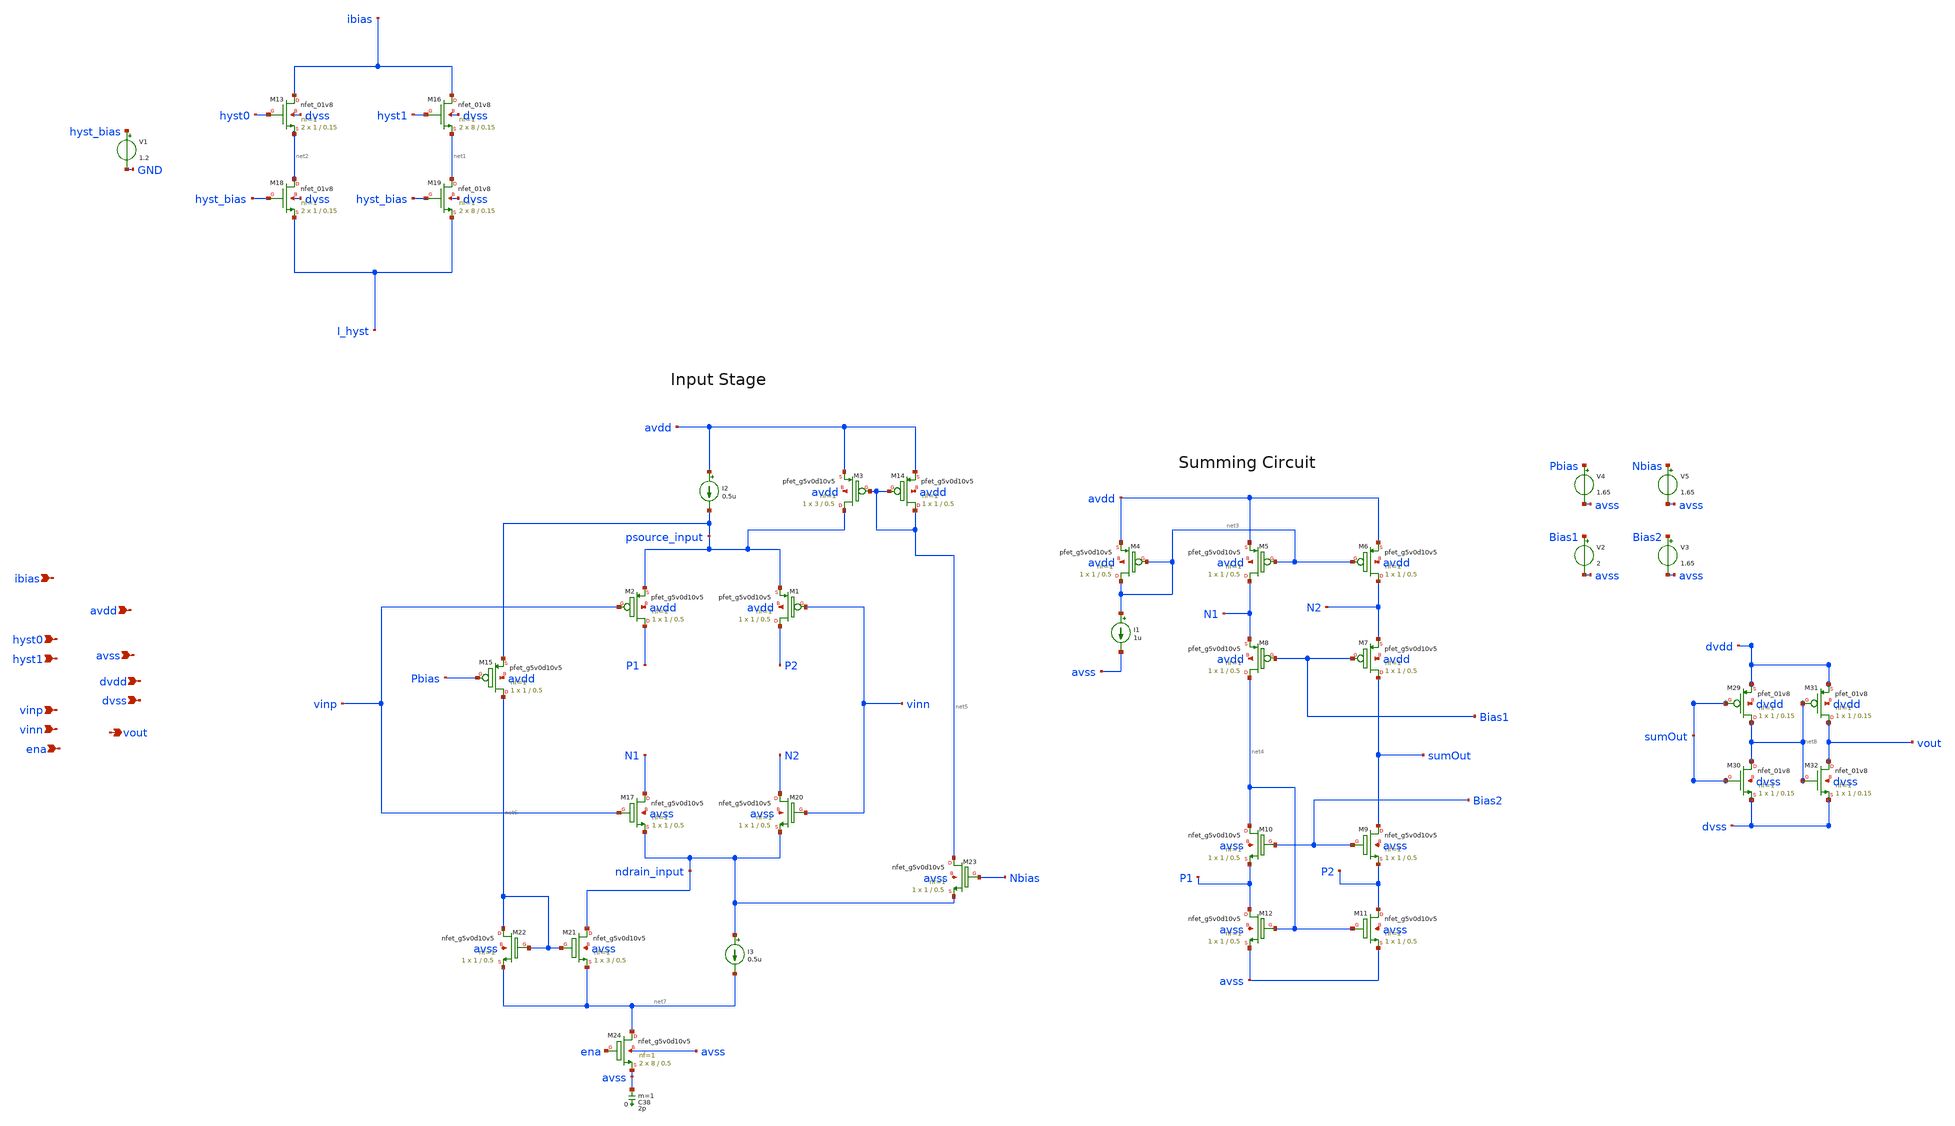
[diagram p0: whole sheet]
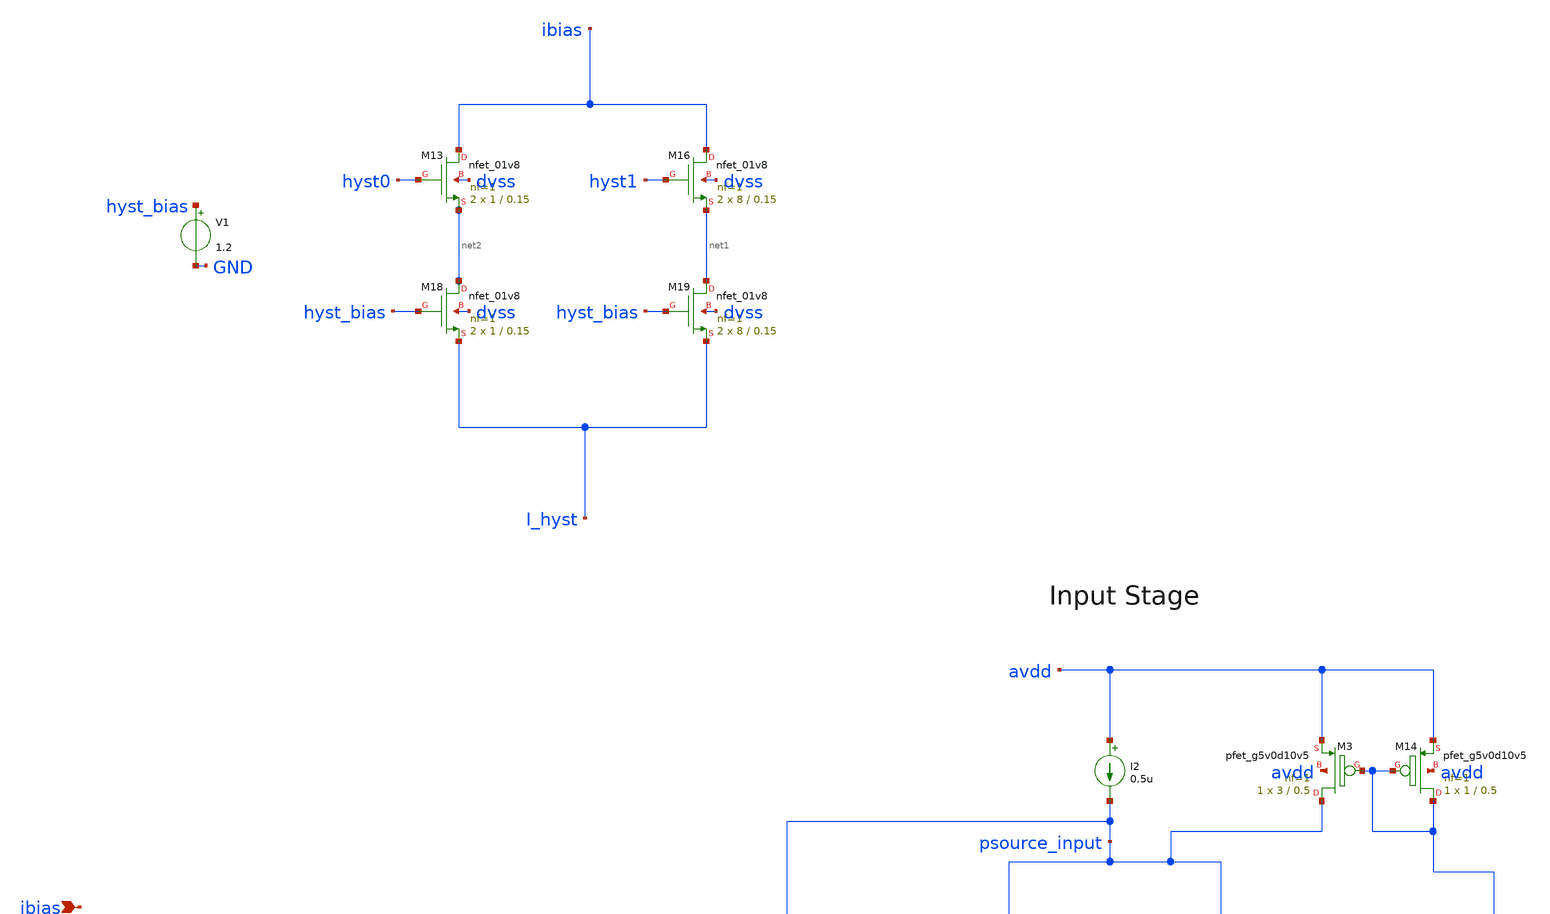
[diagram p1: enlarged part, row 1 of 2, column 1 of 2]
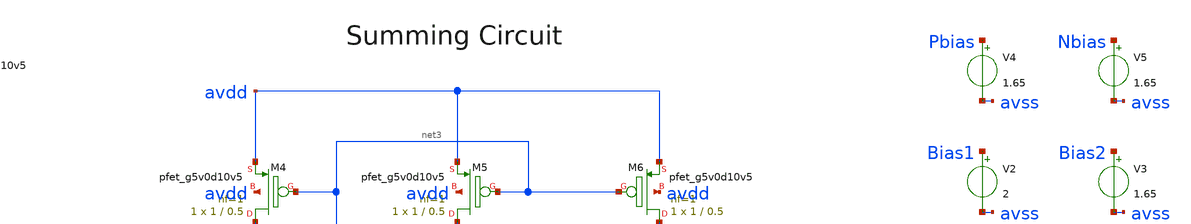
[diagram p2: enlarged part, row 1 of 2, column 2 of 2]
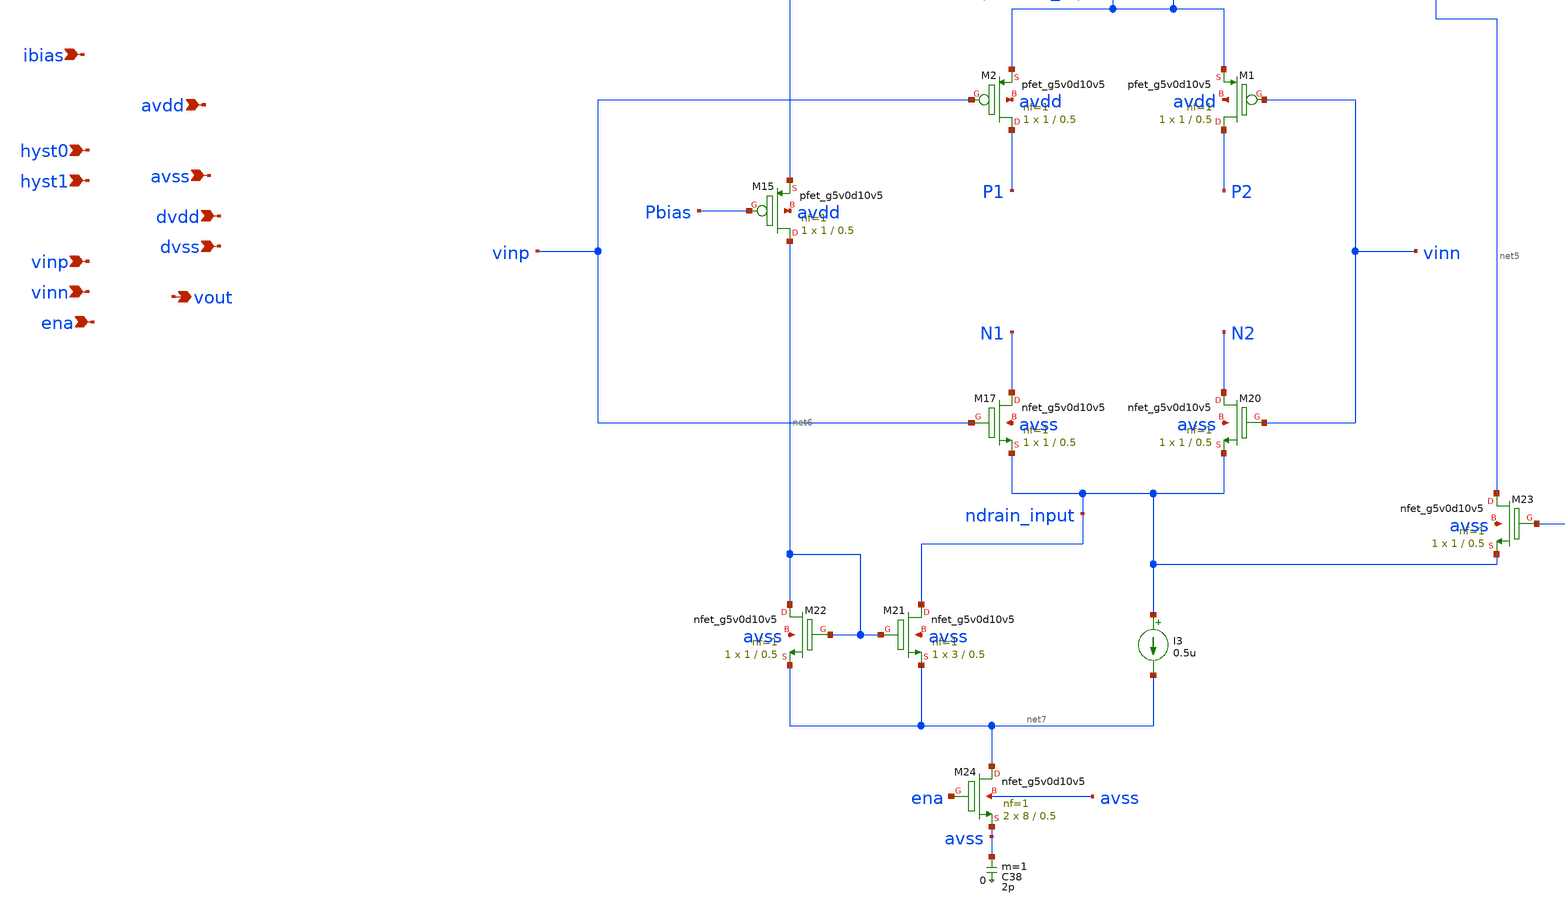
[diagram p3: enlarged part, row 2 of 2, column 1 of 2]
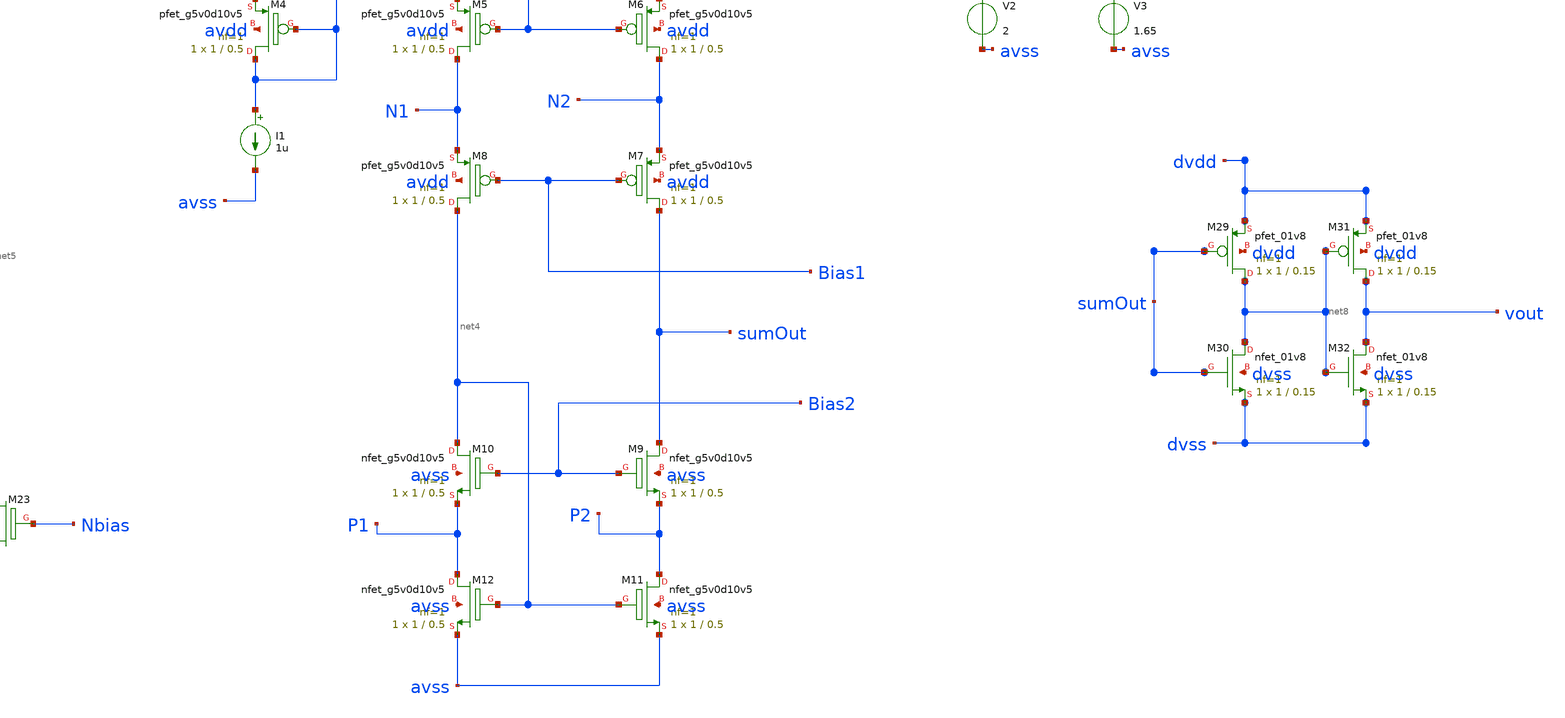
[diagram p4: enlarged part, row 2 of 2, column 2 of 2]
** sch_path: Chipalooza_April2024_Comparator/xschem/Chipalooza_April2024_Comparator(copy2).sch
**.subckt Chipalooza_April2024_Comparator(copy2) vinp vinn hyst0 hyst1 avdd avss dvdd dvss vout ena
*+ ibias
*.ipin vinp
*.ipin vinn
*.ipin hyst0
*.ipin hyst1
*.ipin avdd
*.ipin avss
*.ipin dvdd
*.ipin dvss
*.opin vout
*.ipin ena
*.ipin ibias
XM13 ibias hyst0 net2 dvss sky130_fd_pr__nfet_01v8 L=0.15 W=1 nf=1 ad='int((1 + 1)/2) * 1 / 1 * 0.29'
+ as='int((1 + 2)/2) * 1 / 1 * 0.29' pd='2*int((1 + 1)/2) * (1 / 1 + 0.29)' ps='2*int((1 + 2)/2) * (1 / 1 + 0.29)'
+ nrd='0.29 / 1 ' nrs='0.29 / 1 ' sa=0 sb=0 sd=0 mult=2 m=2
C38 avss 0 2p m=1
XM24 net7 ena avss avss sky130_fd_pr__nfet_g5v0d10v5 L=0.5 W=8 nf=1 ad='int((nf+1)/2) * W/nf * 0.29'
+ as='int((nf+2)/2) * W/nf * 0.29' pd='2*int((nf+1)/2) * (W/nf + 0.29)' ps='2*int((nf+2)/2) * (W/nf + 0.29)'
+ nrd='0.29 / W' nrs='0.29 / W' sa=0 sb=0 sd=0 mult=2 m=2
XM16 ibias hyst1 net1 dvss sky130_fd_pr__nfet_01v8 L=0.15 W=8 nf=1 ad='int((1 + 1)/2) * 8 / 1 * 0.29'
+ as='int((1 + 2)/2) * 8 / 1 * 0.29' pd='2*int((1 + 1)/2) * (8 / 1 + 0.29)' ps='2*int((1 + 2)/2) * (8 / 1 + 0.29)'
+ nrd='0.29 / 8 ' nrs='0.29 / 8 ' sa=0 sb=0 sd=0 mult=2 m=2
XM19 net1 hyst_bias I_hyst dvss sky130_fd_pr__nfet_01v8 L=0.15 W=8 nf=1 ad='int((1 + 1)/2) * 8 / 1 * 0.29'
+ as='int((1 + 2)/2) * 8 / 1 * 0.29' pd='2*int((1 + 1)/2) * (8 / 1 + 0.29)' ps='2*int((1 + 2)/2) * (8 / 1 + 0.29)'
+ nrd='0.29 / 8 ' nrs='0.29 / 8 ' sa=0 sb=0 sd=0 mult=2 m=2
XM18 net2 hyst_bias I_hyst dvss sky130_fd_pr__nfet_01v8 L=0.15 W=1 nf=1 ad='int((1 + 1)/2) * 1 / 1 * 0.29'
+ as='int((1 + 2)/2) * 1 / 1 * 0.29' pd='2*int((1 + 1)/2) * (1 / 1 + 0.29)' ps='2*int((1 + 2)/2) * (1 / 1 + 0.29)'
+ nrd='0.29 / 1 ' nrs='0.29 / 1 ' sa=0 sb=0 sd=0 mult=2 m=2
V1 hyst_bias GND 1.2
XM4 net3 net3 avdd avdd sky130_fd_pr__pfet_g5v0d10v5 L=0.5 W=1 nf=1 ad='int((nf+1)/2) * W/nf * 0.29'
+ as='int((nf+2)/2) * W/nf * 0.29' pd='2*int((nf+1)/2) * (W/nf + 0.29)' ps='2*int((nf+2)/2) * (W/nf + 0.29)'
+ nrd='0.29 / W' nrs='0.29 / W' sa=0 sb=0 sd=0 mult=1 m=1
XM5 N1 net3 avdd avdd sky130_fd_pr__pfet_g5v0d10v5 L=0.5 W=1 nf=1 ad='int((nf+1)/2) * W/nf * 0.29' as='int((nf+2)/2) * W/nf * 0.29'
+ pd='2*int((nf+1)/2) * (W/nf + 0.29)' ps='2*int((nf+2)/2) * (W/nf + 0.29)' nrd='0.29 / W' nrs='0.29 / W'
+ sa=0 sb=0 sd=0 mult=1 m=1
XM6 N2 net3 avdd avdd sky130_fd_pr__pfet_g5v0d10v5 L=0.5 W=1 nf=1 ad='int((nf+1)/2) * W/nf * 0.29' as='int((nf+2)/2) * W/nf * 0.29'
+ pd='2*int((nf+1)/2) * (W/nf + 0.29)' ps='2*int((nf+2)/2) * (W/nf + 0.29)' nrd='0.29 / W' nrs='0.29 / W'
+ sa=0 sb=0 sd=0 mult=1 m=1
XM7 sumOut Bias1 N2 avdd sky130_fd_pr__pfet_g5v0d10v5 L=0.5 W=1 nf=1 ad='int((nf+1)/2) * W/nf * 0.29'
+ as='int((nf+2)/2) * W/nf * 0.29' pd='2*int((nf+1)/2) * (W/nf + 0.29)' ps='2*int((nf+2)/2) * (W/nf + 0.29)'
+ nrd='0.29 / W' nrs='0.29 / W' sa=0 sb=0 sd=0 mult=1 m=1
XM8 net4 Bias1 N1 avdd sky130_fd_pr__pfet_g5v0d10v5 L=0.5 W=1 nf=1 ad='int((nf+1)/2) * W/nf * 0.29' as='int((nf+2)/2) * W/nf * 0.29'
+ pd='2*int((nf+1)/2) * (W/nf + 0.29)' ps='2*int((nf+2)/2) * (W/nf + 0.29)' nrd='0.29 / W' nrs='0.29 / W'
+ sa=0 sb=0 sd=0 mult=1 m=1
XM9 sumOut Bias2 P2 avss sky130_fd_pr__nfet_g5v0d10v5 L=0.5 W=1 nf=1 ad='int((nf+1)/2) * W/nf * 0.29'
+ as='int((nf+2)/2) * W/nf * 0.29' pd='2*int((nf+1)/2) * (W/nf + 0.29)' ps='2*int((nf+2)/2) * (W/nf + 0.29)'
+ nrd='0.29 / W' nrs='0.29 / W' sa=0 sb=0 sd=0 mult=1 m=1
XM10 net4 Bias2 P1 avss sky130_fd_pr__nfet_g5v0d10v5 L=0.5 W=1 nf=1 ad='int((nf+1)/2) * W/nf * 0.29'
+ as='int((nf+2)/2) * W/nf * 0.29' pd='2*int((nf+1)/2) * (W/nf + 0.29)' ps='2*int((nf+2)/2) * (W/nf + 0.29)'
+ nrd='0.29 / W' nrs='0.29 / W' sa=0 sb=0 sd=0 mult=1 m=1
XM11 P2 net4 avss avss sky130_fd_pr__nfet_g5v0d10v5 L=0.5 W=1 nf=1 ad='int((nf+1)/2) * W/nf * 0.29' as='int((nf+2)/2) * W/nf * 0.29'
+ pd='2*int((nf+1)/2) * (W/nf + 0.29)' ps='2*int((nf+2)/2) * (W/nf + 0.29)' nrd='0.29 / W' nrs='0.29 / W'
+ sa=0 sb=0 sd=0 mult=1 m=1
XM12 P1 net4 avss avss sky130_fd_pr__nfet_g5v0d10v5 L=0.5 W=1 nf=1 ad='int((nf+1)/2) * W/nf * 0.29' as='int((nf+2)/2) * W/nf * 0.29'
+ pd='2*int((nf+1)/2) * (W/nf + 0.29)' ps='2*int((nf+2)/2) * (W/nf + 0.29)' nrd='0.29 / W' nrs='0.29 / W'
+ sa=0 sb=0 sd=0 mult=1 m=1
I1 net3 avss 1u
XM1 P2 vinn psource_input avdd sky130_fd_pr__pfet_g5v0d10v5 L=0.5 W=1 nf=1 ad='int((nf+1)/2) * W/nf * 0.29'
+ as='int((nf+2)/2) * W/nf * 0.29' pd='2*int((nf+1)/2) * (W/nf + 0.29)' ps='2*int((nf+2)/2) * (W/nf + 0.29)'
+ nrd='0.29 / W' nrs='0.29 / W' sa=0 sb=0 sd=0 mult=1 m=1
XM2 P1 vinp psource_input avdd sky130_fd_pr__pfet_g5v0d10v5 L=0.5 W=1 nf=1 ad='int((nf+1)/2) * W/nf * 0.29'
+ as='int((nf+2)/2) * W/nf * 0.29' pd='2*int((nf+1)/2) * (W/nf + 0.29)' ps='2*int((nf+2)/2) * (W/nf + 0.29)'
+ nrd='0.29 / W' nrs='0.29 / W' sa=0 sb=0 sd=0 mult=1 m=1
I2 avdd psource_input 0.5u
XM3 psource_input net5 avdd avdd sky130_fd_pr__pfet_g5v0d10v5 L=0.5 W=3 nf=1 ad='int((nf+1)/2) * W/nf * 0.29'
+ as='int((nf+2)/2) * W/nf * 0.29' pd='2*int((nf+1)/2) * (W/nf + 0.29)' ps='2*int((nf+2)/2) * (W/nf + 0.29)'
+ nrd='0.29 / W' nrs='0.29 / W' sa=0 sb=0 sd=0 mult=1 m=1
XM14 net5 net5 avdd avdd sky130_fd_pr__pfet_g5v0d10v5 L=0.5 W=1 nf=1 ad='int((nf+1)/2) * W/nf * 0.29'
+ as='int((nf+2)/2) * W/nf * 0.29' pd='2*int((nf+1)/2) * (W/nf + 0.29)' ps='2*int((nf+2)/2) * (W/nf + 0.29)'
+ nrd='0.29 / W' nrs='0.29 / W' sa=0 sb=0 sd=0 mult=1 m=1
XM15 net6 Pbias psource_input avdd sky130_fd_pr__pfet_g5v0d10v5 L=0.5 W=1 nf=1 ad='int((nf+1)/2) * W/nf * 0.29'
+ as='int((nf+2)/2) * W/nf * 0.29' pd='2*int((nf+1)/2) * (W/nf + 0.29)' ps='2*int((nf+2)/2) * (W/nf + 0.29)'
+ nrd='0.29 / W' nrs='0.29 / W' sa=0 sb=0 sd=0 mult=1 m=1
XM17 N1 vinp ndrain_input avss sky130_fd_pr__nfet_g5v0d10v5 L=0.5 W=1 nf=1 ad='int((nf+1)/2) * W/nf * 0.29'
+ as='int((nf+2)/2) * W/nf * 0.29' pd='2*int((nf+1)/2) * (W/nf + 0.29)' ps='2*int((nf+2)/2) * (W/nf + 0.29)'
+ nrd='0.29 / W' nrs='0.29 / W' sa=0 sb=0 sd=0 mult=1 m=1
XM20 N2 vinn ndrain_input avss sky130_fd_pr__nfet_g5v0d10v5 L=0.5 W=1 nf=1 ad='int((nf+1)/2) * W/nf * 0.29'
+ as='int((nf+2)/2) * W/nf * 0.29' pd='2*int((nf+1)/2) * (W/nf + 0.29)' ps='2*int((nf+2)/2) * (W/nf + 0.29)'
+ nrd='0.29 / W' nrs='0.29 / W' sa=0 sb=0 sd=0 mult=1 m=1
XM21 ndrain_input net6 net7 avss sky130_fd_pr__nfet_g5v0d10v5 L=0.5 W=3 nf=1 ad='int((nf+1)/2) * W/nf * 0.29'
+ as='int((nf+2)/2) * W/nf * 0.29' pd='2*int((nf+1)/2) * (W/nf + 0.29)' ps='2*int((nf+2)/2) * (W/nf + 0.29)'
+ nrd='0.29 / W' nrs='0.29 / W' sa=0 sb=0 sd=0 mult=1 m=1
XM22 net6 net6 net7 avss sky130_fd_pr__nfet_g5v0d10v5 L=0.5 W=1 nf=1 ad='int((nf+1)/2) * W/nf * 0.29'
+ as='int((nf+2)/2) * W/nf * 0.29' pd='2*int((nf+1)/2) * (W/nf + 0.29)' ps='2*int((nf+2)/2) * (W/nf + 0.29)'
+ nrd='0.29 / W' nrs='0.29 / W' sa=0 sb=0 sd=0 mult=1 m=1
I3 ndrain_input net7 0.5u
XM23 net5 Nbias ndrain_input avss sky130_fd_pr__nfet_g5v0d10v5 L=0.5 W=1 nf=1 ad='int((nf+1)/2) * W/nf * 0.29'
+ as='int((nf+2)/2) * W/nf * 0.29' pd='2*int((nf+1)/2) * (W/nf + 0.29)' ps='2*int((nf+2)/2) * (W/nf + 0.29)'
+ nrd='0.29 / W' nrs='0.29 / W' sa=0 sb=0 sd=0 mult=1 m=1
V2 Bias1 avss 2
V3 Bias2 avss 1.65
V4 Pbias avss 1.65
V5 Nbias avss 1.65
XM29 net8 sumOut dvdd dvdd sky130_fd_pr__pfet_01v8 L=0.15 W=1 nf=1 ad='int((nf+1)/2) * W/nf * 0.29' as='int((nf+2)/2) * W/nf * 0.29'
+ pd='2*int((nf+1)/2) * (W/nf + 0.29)' ps='2*int((nf+2)/2) * (W/nf + 0.29)' nrd='0.29 / W' nrs='0.29 / W'
+ sa=0 sb=0 sd=0 mult=1 m=1
XM30 net8 sumOut dvss dvss sky130_fd_pr__nfet_01v8 L=0.15 W=1 nf=1 ad='int((nf+1)/2) * W/nf * 0.29' as='int((nf+2)/2) * W/nf * 0.29'
+ pd='2*int((nf+1)/2) * (W/nf + 0.29)' ps='2*int((nf+2)/2) * (W/nf + 0.29)' nrd='0.29 / W' nrs='0.29 / W'
+ sa=0 sb=0 sd=0 mult=1 m=1
XM31 vout net8 dvdd dvdd sky130_fd_pr__pfet_01v8 L=0.15 W=1 nf=1 ad='int((nf+1)/2) * W/nf * 0.29' as='int((nf+2)/2) * W/nf * 0.29'
+ pd='2*int((nf+1)/2) * (W/nf + 0.29)' ps='2*int((nf+2)/2) * (W/nf + 0.29)' nrd='0.29 / W' nrs='0.29 / W'
+ sa=0 sb=0 sd=0 mult=1 m=1
XM32 vout net8 dvss dvss sky130_fd_pr__nfet_01v8 L=0.15 W=1 nf=1 ad='int((nf+1)/2) * W/nf * 0.29' as='int((nf+2)/2) * W/nf * 0.29'
+ pd='2*int((nf+1)/2) * (W/nf + 0.29)' ps='2*int((nf+2)/2) * (W/nf + 0.29)' nrd='0.29 / W' nrs='0.29 / W'
+ sa=0 sb=0 sd=0 mult=1 m=1
**.ends
.end
